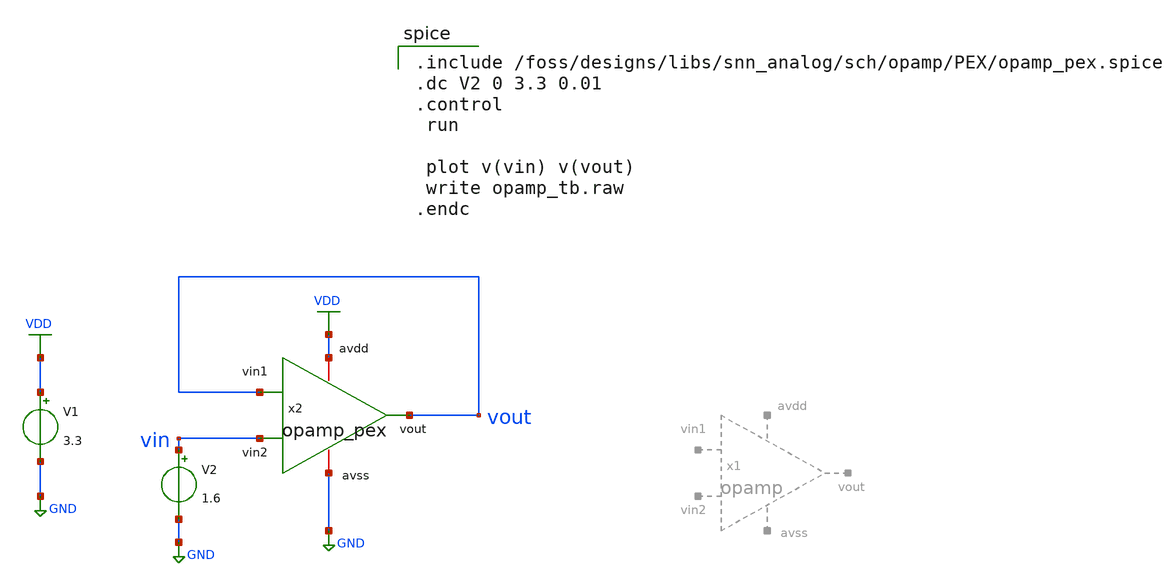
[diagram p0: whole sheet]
** sch_path: designs/libs/snn_analog/sch/opamp/opamp_tb.sch
**.subckt opamp_tb
V1 VDD GND 3.3
V2 vin GND 1.6
x2 VDD vout vin vout GND opamp_pex
**** begin user architecture code

.include /foss/designs/libs/snn_analog/sch/opamp/PEX/opamp_pex.spice
.dc V2 0 3.3 0.01
.control
 run

 plot v(vin) v(vout)
 write opamp_tb.raw
.endc


.include $::180MCU_MODELS/design.ngspice
.lib $::180MCU_MODELS/sm141064.ngspice typical
.lib $::180MCU_MODELS/sm141064.ngspice cap_mim
.lib $::180MCU_MODELS/sm141064.ngspice res_typical
.lib $::180MCU_MODELS/sm141064.ngspice moscap_typical
.lib $::180MCU_MODELS/sm141064.ngspice mimcap_typical
* .lib $::180MCU_MODELS/sm141064.ngspice res_statistical

**** end user architecture code
**.ends
.GLOBAL VDD
.GLOBAL GND
.end
